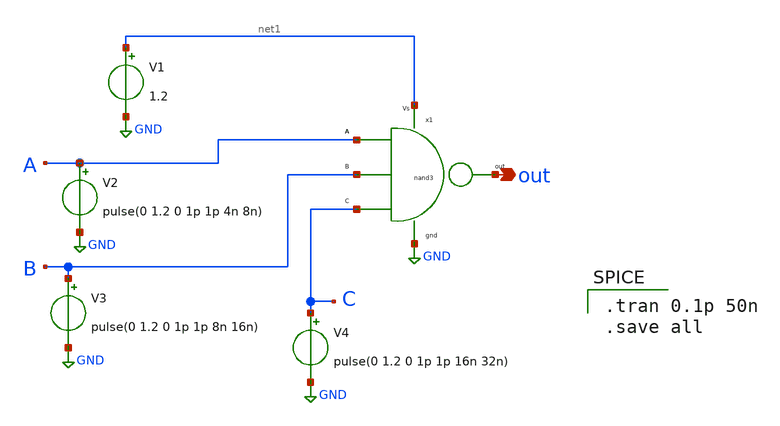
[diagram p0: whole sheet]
** sch_path: component/NAND3/NAND3_sym_test.sch
**.subckt NAND3_sym_test out
*.opin out
V2 A GND pulse(0 1.2 0 1p 1p 4n 8n)
V3 B GND pulse(0 1.2 0 1p 1p 8n 16n)
V4 C GND pulse(0 1.2 0 1p 1p 16n 32n)
V1 net1 GND 1.2
x1 A B C net1 GND out NAND3
**** begin user architecture code

** opencircuitdesign pdks install
.lib $::SKYWATER_MODELS/sky130.lib.spice tt



.tran 0.1p 50n
.save all

**** end user architecture code
**.ends

* expanding   symbol:  Pico_project/NAND3/NAND3.sym # of pins=6
** sym_path: component/NAND3/NAND3.sym
** sch_path: component/NAND3/NAND3.sch
.subckt NAND3 A B C VP VN Y
*.iopin VP
*.iopin VN
*.ipin A
*.ipin B
*.ipin C
*.opin Y
XM1 Y A net1 VN sky130_fd_pr__nfet_01v8 L=0.15 W=1.26 nf=1 ad='int((nf+1)/2) * W/nf * 0.29' as='int((nf+2)/2) * W/nf * 0.29'
+ pd='2*int((nf+1)/2) * (W/nf + 0.29)' ps='2*int((nf+2)/2) * (W/nf + 0.29)' nrd='0.29 / W' nrs='0.29 / W'
+ sa=0 sb=0 sd=0 mult=1 m=1
XM2 net1 B net2 VN sky130_fd_pr__nfet_01v8 L=0.15 W=1.26 nf=1 ad='int((nf+1)/2) * W/nf * 0.29' as='int((nf+2)/2) * W/nf * 0.29'
+ pd='2*int((nf+1)/2) * (W/nf + 0.29)' ps='2*int((nf+2)/2) * (W/nf + 0.29)' nrd='0.29 / W' nrs='0.29 / W'
+ sa=0 sb=0 sd=0 mult=1 m=1
XM3 net2 C VN VN sky130_fd_pr__nfet_01v8 L=0.15 W=1.26 nf=1 ad='int((nf+1)/2) * W/nf * 0.29' as='int((nf+2)/2) * W/nf * 0.29'
+ pd='2*int((nf+1)/2) * (W/nf + 0.29)' ps='2*int((nf+2)/2) * (W/nf + 0.29)' nrd='0.29 / W' nrs='0.29 / W'
+ sa=0 sb=0 sd=0 mult=1 m=1
XM4 Y A VP VP sky130_fd_pr__pfet_01v8 L=0.15 W=1.26 nf=1 ad='int((nf+1)/2) * W/nf * 0.29' as='int((nf+2)/2) * W/nf * 0.29'
+ pd='2*int((nf+1)/2) * (W/nf + 0.29)' ps='2*int((nf+2)/2) * (W/nf + 0.29)' nrd='0.29 / W' nrs='0.29 / W'
+ sa=0 sb=0 sd=0 mult=1 m=1
XM5 Y B VP VP sky130_fd_pr__pfet_01v8 L=0.15 W=1.26 nf=1 ad='int((nf+1)/2) * W/nf * 0.29' as='int((nf+2)/2) * W/nf * 0.29'
+ pd='2*int((nf+1)/2) * (W/nf + 0.29)' ps='2*int((nf+2)/2) * (W/nf + 0.29)' nrd='0.29 / W' nrs='0.29 / W'
+ sa=0 sb=0 sd=0 mult=1 m=1
XM6 Y C VP VP sky130_fd_pr__pfet_01v8 L=0.15 W=1.26 nf=1 ad='int((nf+1)/2) * W/nf * 0.29' as='int((nf+2)/2) * W/nf * 0.29'
+ pd='2*int((nf+1)/2) * (W/nf + 0.29)' ps='2*int((nf+2)/2) * (W/nf + 0.29)' nrd='0.29 / W' nrs='0.29 / W'
+ sa=0 sb=0 sd=0 mult=1 m=1
.ends

.GLOBAL GND
.end
